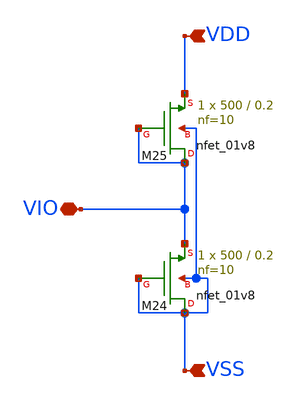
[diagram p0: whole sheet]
** sch_path: flashADC/xschem/ESD.sch
**.subckt ESD VSS VDD VIO
*.ipin VSS
*.ipin VDD
*.iopin VIO
XM24 VSS VSS VIO VSS sky130_fd_pr__nfet_01v8 L=0.2 W=500 nf=10 ad='int((nf+1)/2) * W/nf * 0.29' as='int((nf+2)/2) * W/nf * 0.29'
+ pd='2*int((nf+1)/2) * (W/nf + 0.29)' ps='2*int((nf+2)/2) * (W/nf + 0.29)' nrd='0.29 / W' nrs='0.29 / W'
+ sa=0 sb=0 sd=0 mult=1 m=1
XM25 VIO VIO VDD VSS sky130_fd_pr__nfet_01v8 L=0.2 W=500 nf=10 ad='int((nf+1)/2) * W/nf * 0.29' as='int((nf+2)/2) * W/nf * 0.29'
+ pd='2*int((nf+1)/2) * (W/nf + 0.29)' ps='2*int((nf+2)/2) * (W/nf + 0.29)' nrd='0.29 / W' nrs='0.29 / W'
+ sa=0 sb=0 sd=0 mult=1 m=1
**.ends
.end
